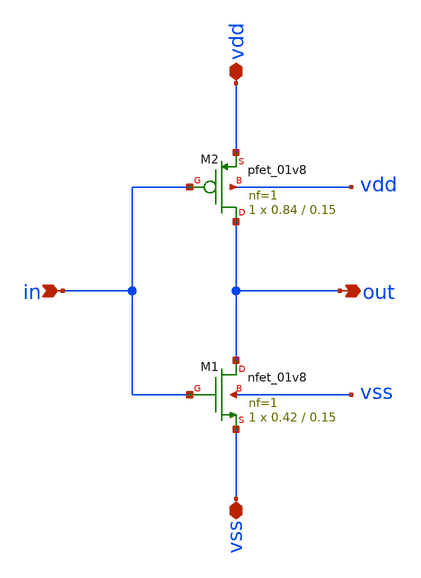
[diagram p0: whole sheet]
** sch_path: xschem/afernandez_residue_amplifier/inverter_min.sch
**.subckt inverter_min vss in out vdd
*.iopin vss
*.ipin in
*.opin out
*.iopin vdd
XM2 out in vdd vdd sky130_fd_pr__pfet_01v8 L=0.15 W=0.84 nf=1 ad='int((nf+1)/2) * W/nf * 0.29' as='int((nf+2)/2) * W/nf * 0.29'
+ pd='2*int((nf+1)/2) * (W/nf + 0.29)' ps='2*int((nf+2)/2) * (W/nf + 0.29)' nrd='0.29 / W' nrs='0.29 / W'
+ sa=0 sb=0 sd=0 mult=1 m=1
XM1 out in vss vss sky130_fd_pr__nfet_01v8 L=0.15 W=0.42 nf=1 ad='int((nf+1)/2) * W/nf * 0.29' as='int((nf+2)/2) * W/nf * 0.29'
+ pd='2*int((nf+1)/2) * (W/nf + 0.29)' ps='2*int((nf+2)/2) * (W/nf + 0.29)' nrd='0.29 / W' nrs='0.29 / W'
+ sa=0 sb=0 sd=0 mult=1 m=1
**.ends
.end
